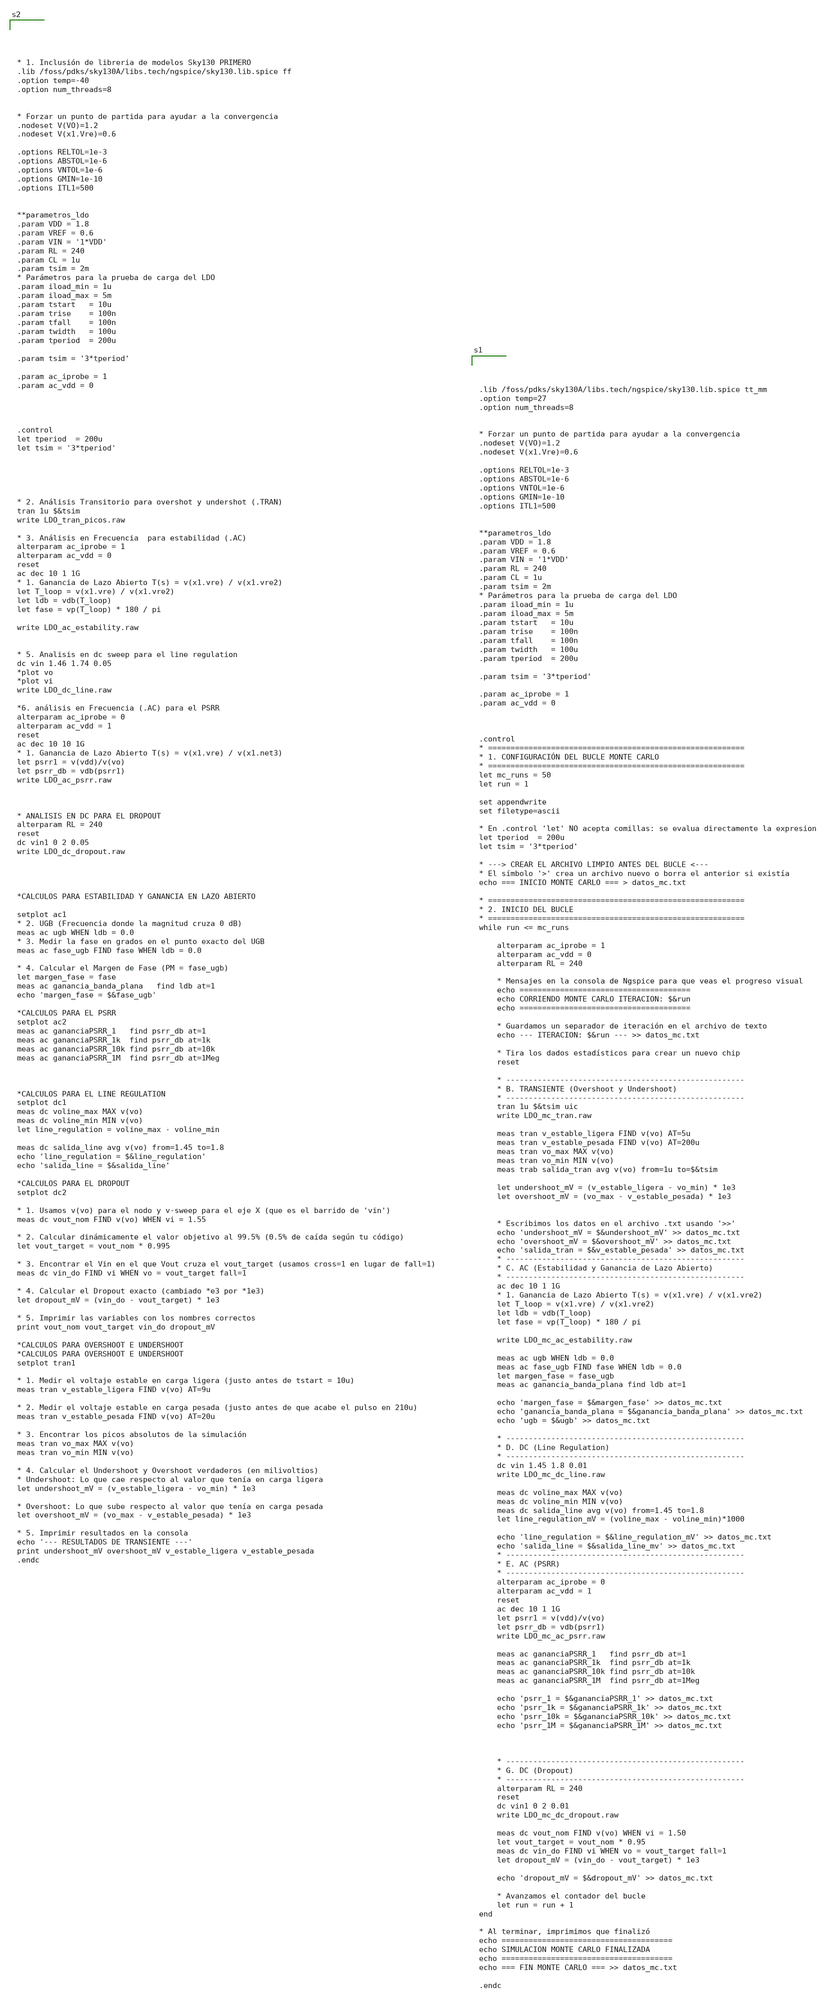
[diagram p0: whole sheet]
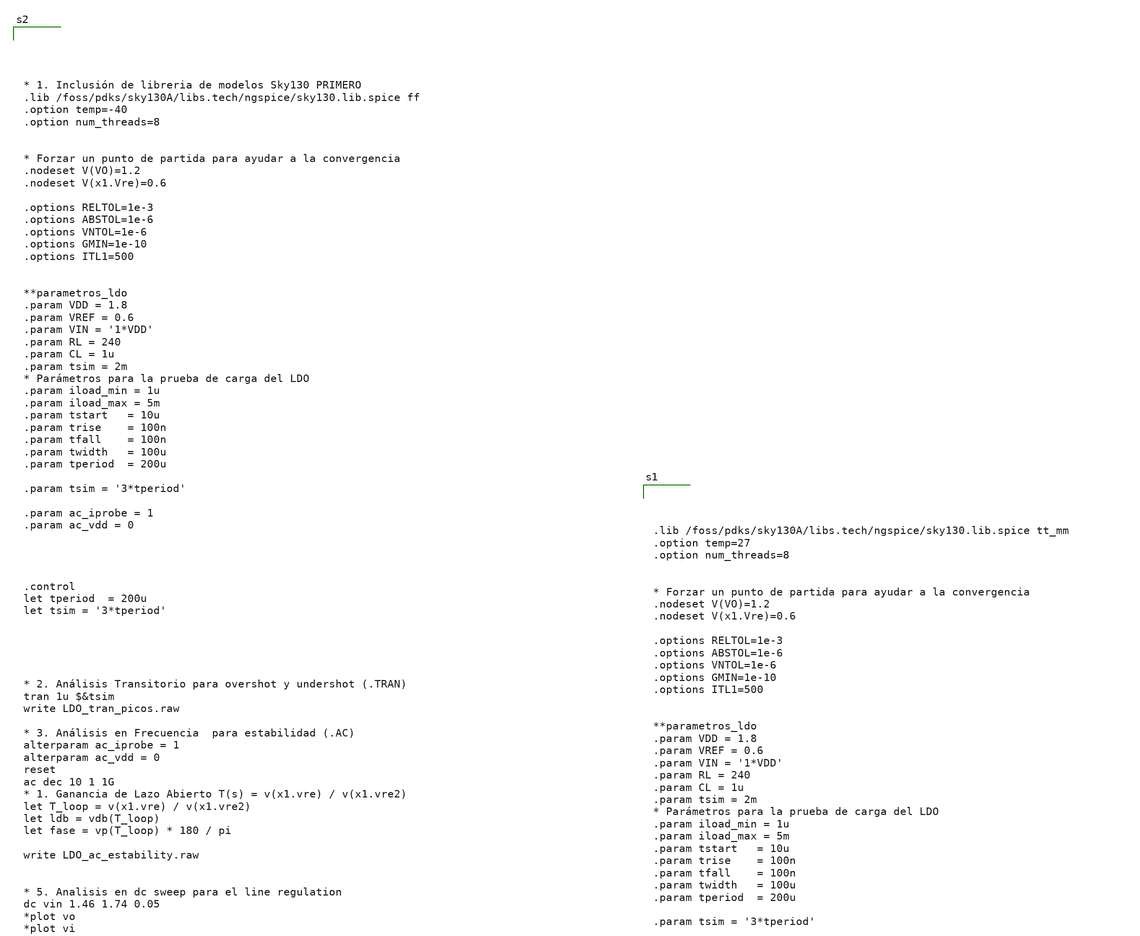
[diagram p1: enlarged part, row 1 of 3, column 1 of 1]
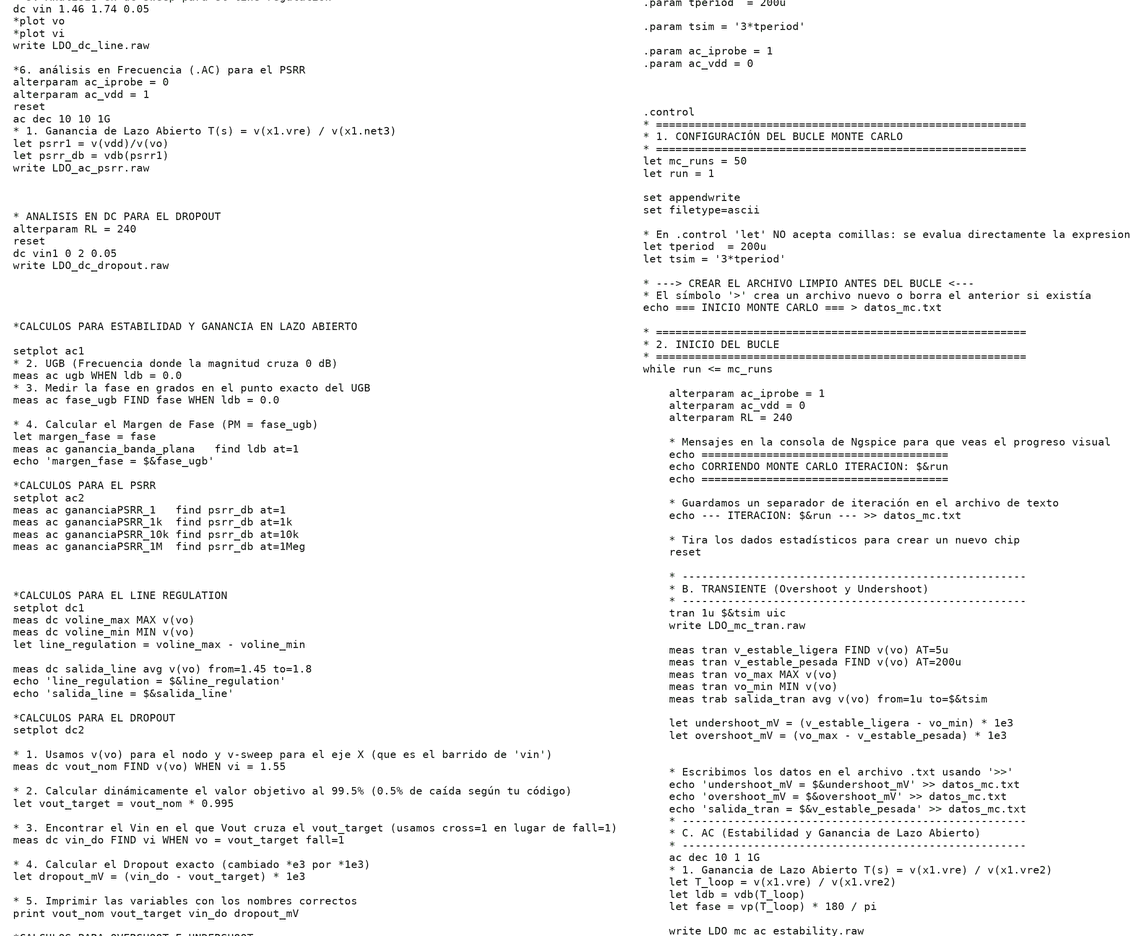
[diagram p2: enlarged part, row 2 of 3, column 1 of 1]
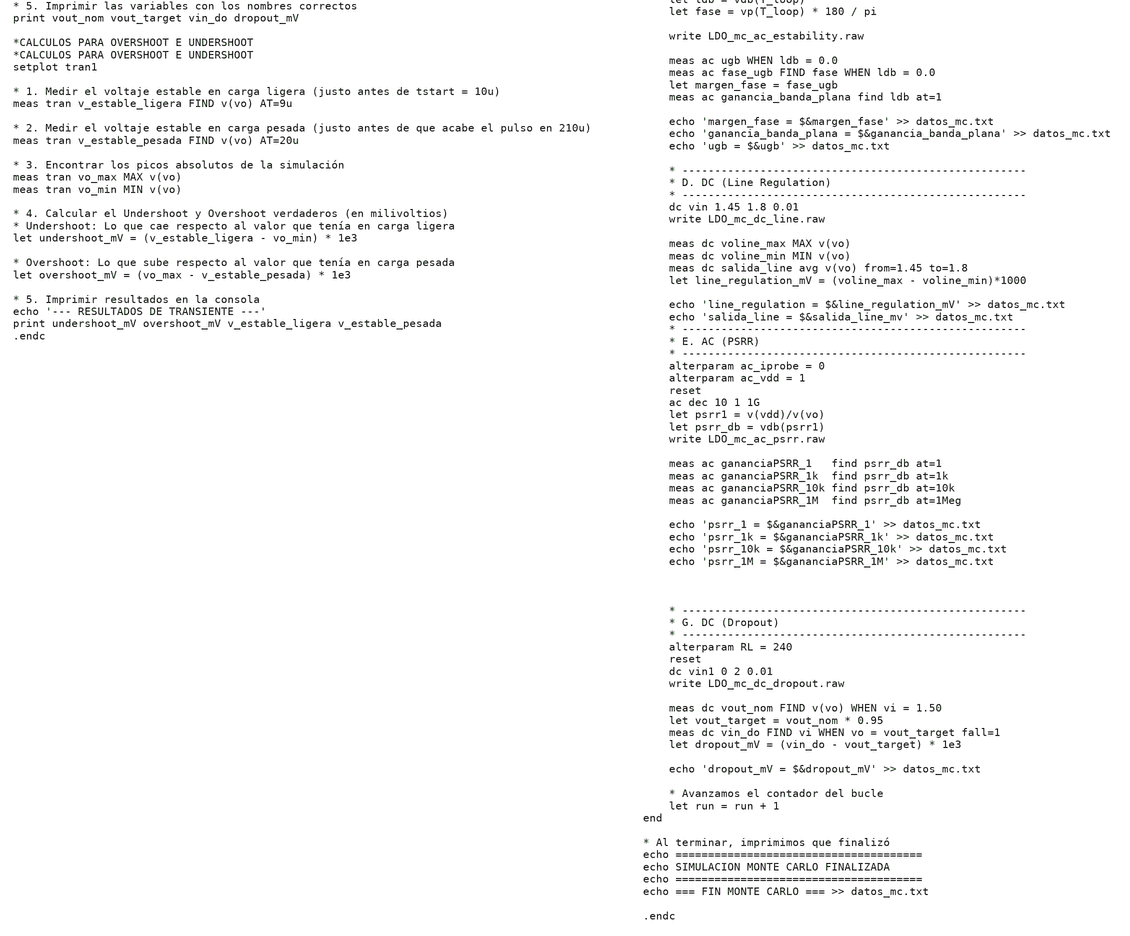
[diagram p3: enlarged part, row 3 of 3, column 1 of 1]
** sch_path: untitled-1.sch
**.subckt untitled-1
**** begin user architecture code




.lib /foss/pdks/sky130A/libs.tech/ngspice/sky130.lib.spice tt_mm
.option temp=27
.option num_threads=8


* Forzar un punto de partida para ayudar a la convergencia
.nodeset V(VO)=1.2
.nodeset V(x1.Vre)=0.6

.options RELTOL=1e-3
.options ABSTOL=1e-6
.options VNTOL=1e-6
.options GMIN=1e-10
.options ITL1=500


**parametros_ldo
.param VDD = 1.8
.param VREF = 0.6
.param VIN = '1*VDD'
.param RL = 240
.param CL = 1u
.param tsim = 2m
* Parámetros para la prueba de carga del LDO
.param iload_min = 1u
.param iload_max = 5m
.param tstart   = 10u
.param trise    = 100n
.param tfall    = 100n
.param twidth   = 100u
.param tperiod  = 200u

.param tsim = '3*tperiod'

.param ac_iprobe = 1
.param ac_vdd = 0



.control
* =========================================================
* 1. CONFIGURACIÓN DEL BUCLE MONTE CARLO
* =========================================================
let mc_runs = 50
let run = 1

set appendwrite
set filetype=ascii

* En .control 'let' NO acepta comillas: se evalua directamente la expresion
let tperiod  = 200u
let tsim = '3*tperiod'

* ---> CREAR EL ARCHIVO LIMPIO ANTES DEL BUCLE <---
* El símbolo '>' crea un archivo nuevo o borra el anterior si existía
echo === INICIO MONTE CARLO === > datos_mc.txt

* =========================================================
* 2. INICIO DEL BUCLE
* =========================================================
while run <= mc_runs

    alterparam ac_iprobe = 1
    alterparam ac_vdd = 0
    alterparam RL = 240

    * Mensajes en la consola de Ngspice para que veas el progreso visual
    echo ======================================
    echo CORRIENDO MONTE CARLO ITERACION: $&run
    echo ======================================

    * Guardamos un separador de iteración en el archivo de texto
    echo --- ITERACION: $&run --- >> datos_mc.txt

    * Tira los dados estadísticos para crear un nuevo chip
    reset

    * -----------------------------------------------------
    * B. TRANSIENTE (Overshoot y Undershoot)
    * -----------------------------------------------------
    tran 1u $&tsim uic
    write LDO_mc_tran.raw

    meas tran v_estable_ligera FIND v(vo) AT=5u
    meas tran v_estable_pesada FIND v(vo) AT=200u
    meas tran vo_max MAX v(vo)
    meas tran vo_min MIN v(vo)
    meas trab salida_tran avg v(vo) from=1u to=$&tsim

    let undershoot_mV = (v_estable_ligera - vo_min) * 1e3
    let overshoot_mV = (vo_max - v_estable_pesada) * 1e3


    * Escribimos los datos en el archivo .txt usando '>>'
    echo 'undershoot_mV = $&undershoot_mV' >> datos_mc.txt
    echo 'overshoot_mV = $&overshoot_mV' >> datos_mc.txt
    echo 'salida_tran = $&v_estable_pesada' >> datos_mc.txt
    * -----------------------------------------------------
    * C. AC (Estabilidad y Ganancia de Lazo Abierto)
    * -----------------------------------------------------
    ac dec 10 1 1G
    * 1. Ganancia de Lazo Abierto T(s) = v(x1.vre) / v(x1.vre2)
    let T_loop = v(x1.vre) / v(x1.vre2)
    let ldb = vdb(T_loop)
    let fase = vp(T_loop) * 180 / pi

    write LDO_mc_ac_estability.raw

    meas ac ugb WHEN ldb = 0.0
    meas ac fase_ugb FIND fase WHEN ldb = 0.0
    let margen_fase = fase_ugb
    meas ac ganancia_banda_plana find ldb at=1

    echo 'margen_fase = $&margen_fase' >> datos_mc.txt
    echo 'ganancia_banda_plana = $&ganancia_banda_plana' >> datos_mc.txt
    echo 'ugb = $&ugb' >> datos_mc.txt

    * -----------------------------------------------------
    * D. DC (Line Regulation)
    * -----------------------------------------------------
    dc vin 1.45 1.8 0.01
    write LDO_mc_dc_line.raw

    meas dc voline_max MAX v(vo)
    meas dc voline_min MIN v(vo)
    meas dc salida_line avg v(vo) from=1.45 to=1.8
    let line_regulation_mV = (voline_max - voline_min)*1000

    echo 'line_regulation = $&line_regulation_mV' >> datos_mc.txt
    echo 'salida_line = $&salida_line_mv' >> datos_mc.txt
    * -----------------------------------------------------
    * E. AC (PSRR)
    * -----------------------------------------------------
    alterparam ac_iprobe = 0
    alterparam ac_vdd = 1
    reset
    ac dec 10 1 1G
    let psrr1 = v(vdd)/v(vo)
    let psrr_db = vdb(psrr1)
    write LDO_mc_ac_psrr.raw

    meas ac gananciaPSRR_1   find psrr_db at=1
    meas ac gananciaPSRR_1k  find psrr_db at=1k
    meas ac gananciaPSRR_10k find psrr_db at=10k
    meas ac gananciaPSRR_1M  find psrr_db at=1Meg

    echo 'psrr_1 = $&gananciaPSRR_1' >> datos_mc.txt
    echo 'psrr_1k = $&gananciaPSRR_1k' >> datos_mc.txt
    echo 'psrr_10k = $&gananciaPSRR_10k' >> datos_mc.txt
    echo 'psrr_1M = $&gananciaPSRR_1M' >> datos_mc.txt



    * -----------------------------------------------------
    * G. DC (Dropout)
    * -----------------------------------------------------
    alterparam RL = 240
    reset
    dc vin1 0 2 0.01
    write LDO_mc_dc_dropout.raw

    meas dc vout_nom FIND v(vo) WHEN vi = 1.50
    let vout_target = vout_nom * 0.95
    meas dc vin_do FIND vi WHEN vo = vout_target fall=1
    let dropout_mV = (vin_do - vout_target) * 1e3

    echo 'dropout_mV = $&dropout_mV' >> datos_mc.txt

    * Avanzamos el contador del bucle
    let run = run + 1
end

* Al terminar, imprimimos que finalizó
echo ======================================
echo SIMULACION MONTE CARLO FINALIZADA
echo ======================================
echo === FIN MONTE CARLO === >> datos_mc.txt

.endc








* 1. Inclusión de libreria de modelos Sky130 PRIMERO
.lib /foss/pdks/sky130A/libs.tech/ngspice/sky130.lib.spice ff
.option temp=-40
.option num_threads=8


* Forzar un punto de partida para ayudar a la convergencia
.nodeset V(VO)=1.2
.nodeset V(x1.Vre)=0.6

.options RELTOL=1e-3
.options ABSTOL=1e-6
.options VNTOL=1e-6
.options GMIN=1e-10
.options ITL1=500


**parametros_ldo
.param VDD = 1.8
.param VREF = 0.6
.param VIN = '1*VDD'
.param RL = 240
.param CL = 1u
.param tsim = 2m
* Parámetros para la prueba de carga del LDO
.param iload_min = 1u
.param iload_max = 5m
.param tstart   = 10u
.param trise    = 100n
.param tfall    = 100n
.param twidth   = 100u
.param tperiod  = 200u

.param tsim = '3*tperiod'

.param ac_iprobe = 1
.param ac_vdd = 0




.control
let tperiod  = 200u
let tsim = '3*tperiod'





* 2. Análisis Transitorio para overshot y undershot (.TRAN)
tran 1u $&tsim
write LDO_tran_picos.raw

* 3. Análisis en Frecuencia  para estabilidad (.AC)
alterparam ac_iprobe = 1
alterparam ac_vdd = 0
reset
ac dec 10 1 1G
* 1. Ganancia de Lazo Abierto T(s) = v(x1.vre) / v(x1.vre2)
let T_loop = v(x1.vre) / v(x1.vre2)
let ldb = vdb(T_loop)
let fase = vp(T_loop) * 180 / pi

write LDO_ac_estability.raw


* 5. Analisis en dc sweep para el line regulation
dc vin 1.46 1.74 0.05
*plot vo
*plot vi
write LDO_dc_line.raw

*6. análisis en Frecuencia (.AC) para el PSRR
alterparam ac_iprobe = 0
alterparam ac_vdd = 1
reset
ac dec 10 10 1G
* 1. Ganancia de Lazo Abierto T(s) = v(x1.vre) / v(x1.net3)
let psrr1 = v(vdd)/v(vo)
let psrr_db = vdb(psrr1)
write LDO_ac_psrr.raw



* ANALISIS EN DC PARA EL DROPOUT
alterparam RL = 240
reset
dc vin1 0 2 0.05
write LDO_dc_dropout.raw




*CALCULOS PARA ESTABILIDAD Y GANANCIA EN LAZO ABIERTO

setplot ac1
* 2. UGB (Frecuencia donde la magnitud cruza 0 dB)
meas ac ugb WHEN ldb = 0.0
* 3. Medir la fase en grados en el punto exacto del UGB
meas ac fase_ugb FIND fase WHEN ldb = 0.0

* 4. Calcular el Margen de Fase (PM = fase_ugb)
let margen_fase = fase
meas ac ganancia_banda_plana   find ldb at=1
echo 'margen_fase = $&fase_ugb'

*CALCULOS PARA EL PSRR
setplot ac2
meas ac gananciaPSRR_1   find psrr_db at=1
meas ac gananciaPSRR_1k  find psrr_db at=1k
meas ac gananciaPSRR_10k find psrr_db at=10k
meas ac gananciaPSRR_1M  find psrr_db at=1Meg



*CALCULOS PARA EL LINE REGULATION
setplot dc1
meas dc voline_max MAX v(vo)
meas dc voline_min MIN v(vo)
let line_regulation = voline_max - voline_min

meas dc salida_line avg v(vo) from=1.45 to=1.8
echo 'line_regulation = $&line_regulation'
echo 'salida_line = $&salida_line'

*CALCULOS PARA EL DROPOUT
setplot dc2

* 1. Usamos v(vo) para el nodo y v-sweep para el eje X (que es el barrido de 'vin')
meas dc vout_nom FIND v(vo) WHEN vi = 1.55

* 2. Calcular dinámicamente el valor objetivo al 99.5% (0.5% de caída según tu código)
let vout_target = vout_nom * 0.995

* 3. Encontrar el Vin en el que Vout cruza el vout_target (usamos cross=1 en lugar de fall=1)
meas dc vin_do FIND vi WHEN vo = vout_target fall=1

* 4. Calcular el Dropout exacto (cambiado *e3 por *1e3)
let dropout_mV = (vin_do - vout_target) * 1e3

* 5. Imprimir las variables con los nombres correctos
print vout_nom vout_target vin_do dropout_mV

*CALCULOS PARA OVERSHOOT E UNDERSHOOT
*CALCULOS PARA OVERSHOOT E UNDERSHOOT
setplot tran1

* 1. Medir el voltaje estable en carga ligera (justo antes de tstart = 10u)
meas tran v_estable_ligera FIND v(vo) AT=9u

* 2. Medir el voltaje estable en carga pesada (justo antes de que acabe el pulso en 210u)
meas tran v_estable_pesada FIND v(vo) AT=20u

* 3. Encontrar los picos absolutos de la simulación
meas tran vo_max MAX v(vo)
meas tran vo_min MIN v(vo)

* 4. Calcular el Undershoot y Overshoot verdaderos (en milivoltios)
* Undershoot: Lo que cae respecto al valor que tenía en carga ligera
let undershoot_mV = (v_estable_ligera - vo_min) * 1e3

* Overshoot: Lo que sube respecto al valor que tenía en carga pesada
let overshoot_mV = (vo_max - v_estable_pesada) * 1e3

* 5. Imprimir resultados en la consola
echo '--- RESULTADOS DE TRANSIENTE ---'
print undershoot_mV overshoot_mV v_estable_ligera v_estable_pesada
.endc



**** end user architecture code
**.ends
.end
